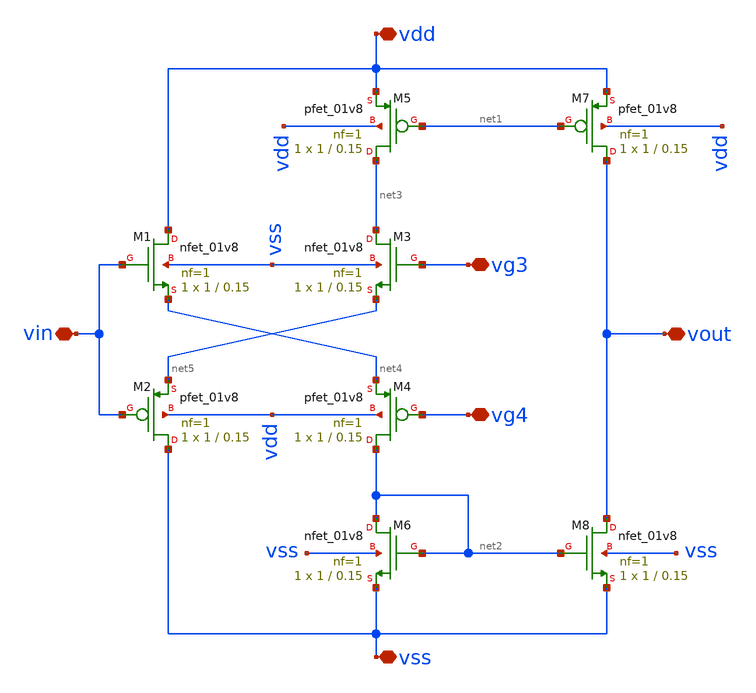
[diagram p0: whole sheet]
** sch_path: Synapse/PushPull.sch
**.subckt PushPull vout vin vg3 vg4 vdd vss
*.iopin vout
*.iopin vin
*.iopin vg3
*.iopin vg4
*.iopin vdd
*.iopin vss
XM1 vdd vin net4 vss sky130_fd_pr__nfet_01v8 L=0.15 W=1 nf=1 ad='int((nf+1)/2) * W/nf * 0.29' as='int((nf+2)/2) * W/nf * 0.29'
+ pd='2*int((nf+1)/2) * (W/nf + 0.29)' ps='2*int((nf+2)/2) * (W/nf + 0.29)' nrd='0.29 / W' nrs='0.29 / W'
+ sa=0 sb=0 sd=0 mult=1 m=1
XM2 vss vin net5 vdd sky130_fd_pr__pfet_01v8 L=0.15 W=1 nf=1 ad='int((nf+1)/2) * W/nf * 0.29' as='int((nf+2)/2) * W/nf * 0.29'
+ pd='2*int((nf+1)/2) * (W/nf + 0.29)' ps='2*int((nf+2)/2) * (W/nf + 0.29)' nrd='0.29 / W' nrs='0.29 / W'
+ sa=0 sb=0 sd=0 mult=1 m=1
XM3 net3 vg3 net5 vss sky130_fd_pr__nfet_01v8 L=0.15 W=1 nf=1 ad='int((nf+1)/2) * W/nf * 0.29' as='int((nf+2)/2) * W/nf * 0.29'
+ pd='2*int((nf+1)/2) * (W/nf + 0.29)' ps='2*int((nf+2)/2) * (W/nf + 0.29)' nrd='0.29 / W' nrs='0.29 / W'
+ sa=0 sb=0 sd=0 mult=1 m=1
XM4 net2 vg4 net4 vdd sky130_fd_pr__pfet_01v8 L=0.15 W=1 nf=1 ad='int((nf+1)/2) * W/nf * 0.29' as='int((nf+2)/2) * W/nf * 0.29'
+ pd='2*int((nf+1)/2) * (W/nf + 0.29)' ps='2*int((nf+2)/2) * (W/nf + 0.29)' nrd='0.29 / W' nrs='0.29 / W'
+ sa=0 sb=0 sd=0 mult=1 m=1
XM5 net3 net1 vdd vdd sky130_fd_pr__pfet_01v8 L=0.15 W=1 nf=1 ad='int((nf+1)/2) * W/nf * 0.29' as='int((nf+2)/2) * W/nf * 0.29'
+ pd='2*int((nf+1)/2) * (W/nf + 0.29)' ps='2*int((nf+2)/2) * (W/nf + 0.29)' nrd='0.29 / W' nrs='0.29 / W'
+ sa=0 sb=0 sd=0 mult=1 m=1
XM6 net2 net2 vss vss sky130_fd_pr__nfet_01v8 L=0.15 W=1 nf=1 ad='int((nf+1)/2) * W/nf * 0.29' as='int((nf+2)/2) * W/nf * 0.29'
+ pd='2*int((nf+1)/2) * (W/nf + 0.29)' ps='2*int((nf+2)/2) * (W/nf + 0.29)' nrd='0.29 / W' nrs='0.29 / W'
+ sa=0 sb=0 sd=0 mult=1 m=1
XM7 vout net1 vdd vdd sky130_fd_pr__pfet_01v8 L=0.15 W=1 nf=1 ad='int((nf+1)/2) * W/nf * 0.29' as='int((nf+2)/2) * W/nf * 0.29'
+ pd='2*int((nf+1)/2) * (W/nf + 0.29)' ps='2*int((nf+2)/2) * (W/nf + 0.29)' nrd='0.29 / W' nrs='0.29 / W'
+ sa=0 sb=0 sd=0 mult=1 m=1
XM8 vout net2 vss vss sky130_fd_pr__nfet_01v8 L=0.15 W=1 nf=1 ad='int((nf+1)/2) * W/nf * 0.29' as='int((nf+2)/2) * W/nf * 0.29'
+ pd='2*int((nf+1)/2) * (W/nf + 0.29)' ps='2*int((nf+2)/2) * (W/nf + 0.29)' nrd='0.29 / W' nrs='0.29 / W'
+ sa=0 sb=0 sd=0 mult=1 m=1
**.ends
.end
